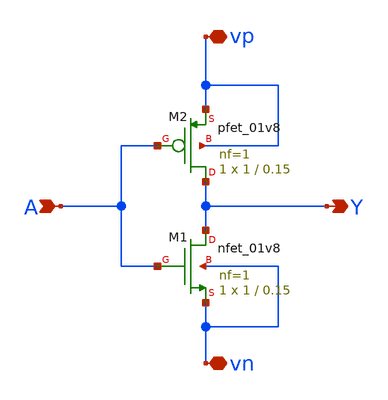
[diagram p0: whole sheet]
** sch_path: VLSI/PROVA_01/Simulazione postlayout/not_1.sch
**.subckt not_1 A vp vn Y
*.ipin A
*.iopin vp
*.iopin vn
*.opin Y
XM1 Y A vn vn sky130_fd_pr__nfet_01v8 L=0.15 W=1 nf=1 ad='int((nf+1)/2) * W/nf * 0.29' as='int((nf+2)/2) * W/nf * 0.29'
+ pd='2*int((nf+1)/2) * (W/nf + 0.29)' ps='2*int((nf+2)/2) * (W/nf + 0.29)' nrd='0.29 / W' nrs='0.29 / W'
+ sa=0 sb=0 sd=0 mult=1 m=1
XM2 Y A vp vp sky130_fd_pr__pfet_01v8 L=0.15 W=1 nf=1 ad='int((nf+1)/2) * W/nf * 0.29' as='int((nf+2)/2) * W/nf * 0.29'
+ pd='2*int((nf+1)/2) * (W/nf + 0.29)' ps='2*int((nf+2)/2) * (W/nf + 0.29)' nrd='0.29 / W' nrs='0.29 / W'
+ sa=0 sb=0 sd=0 mult=1 m=1
**.ends
.end
